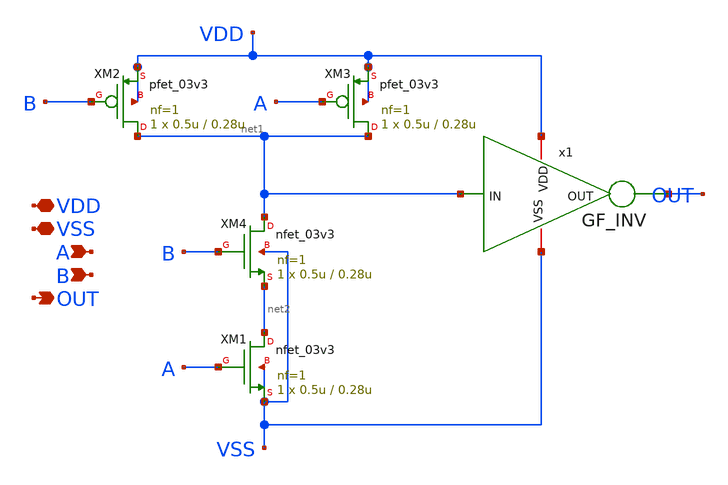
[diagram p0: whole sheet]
** sch_path: DAC_PAKISTAN_01/Pakistan1_Xschem/AND.sch
**.subckt AND VDD VSS A B OUT
*.iopin VDD
*.iopin VSS
*.ipin A
*.ipin B
*.opin OUT
XM1 net2 A VSS VSS nfet_03v3 L=0.28u W=0.5u nf=1 ad='int((nf+1)/2) * W/nf * 0.18u' as='int((nf+2)/2) * W/nf * 0.18u'
+ pd='2*int((nf+1)/2) * (W/nf + 0.18u)' ps='2*int((nf+2)/2) * (W/nf + 0.18u)' nrd='0.18u / W' nrs='0.18u / W'
+ sa=0 sb=0 sd=0 m=1
XM2 net1 B VDD VDD pfet_03v3 L=0.28u W=0.5u nf=1 ad='int((nf+1)/2) * W/nf * 0.18u' as='int((nf+2)/2) * W/nf * 0.18u'
+ pd='2*int((nf+1)/2) * (W/nf + 0.18u)' ps='2*int((nf+2)/2) * (W/nf + 0.18u)' nrd='0.18u / W' nrs='0.18u / W'
+ sa=0 sb=0 sd=0 m=1
XM3 net1 A VDD VDD pfet_03v3 L=0.28u W=0.5u nf=1 ad='int((nf+1)/2) * W/nf * 0.18u' as='int((nf+2)/2) * W/nf * 0.18u'
+ pd='2*int((nf+1)/2) * (W/nf + 0.18u)' ps='2*int((nf+2)/2) * (W/nf + 0.18u)' nrd='0.18u / W' nrs='0.18u / W'
+ sa=0 sb=0 sd=0 m=1
XM4 net1 B net2 VSS nfet_03v3 L=0.28u W=0.5u nf=1 ad='int((nf+1)/2) * W/nf * 0.18u' as='int((nf+2)/2) * W/nf * 0.18u'
+ pd='2*int((nf+1)/2) * (W/nf + 0.18u)' ps='2*int((nf+2)/2) * (W/nf + 0.18u)' nrd='0.18u / W' nrs='0.18u / W'
+ sa=0 sb=0 sd=0 m=1
x1 VSS VDD OUT net1 GF_INV
**.ends

* expanding   symbol:  GF_INV.sym # of pins=4
** sym_path: GF_INV.sym
** sch_path: GF_INV.sch
.subckt GF_INV VSS VDD OUT IN
*.iopin VDD
*.iopin VSS
*.ipin IN
*.opin OUT
XM1 OUT IN VSS VSS nfet_03v3 L=0.28u W=0.25u nf=1 ad='int((nf+1)/2) * W/nf * 0.18u' as='int((nf+2)/2) * W/nf * 0.18u'
+ pd='2*int((nf+1)/2) * (W/nf + 0.18u)' ps='2*int((nf+2)/2) * (W/nf + 0.18u)' nrd='0.18u / W' nrs='0.18u / W'
+ sa=0 sb=0 sd=0 m=1
XM2 OUT IN VDD VDD pfet_03v3 L=0.28u W=0.5u nf=1 ad='int((nf+1)/2) * W/nf * 0.18u' as='int((nf+2)/2) * W/nf * 0.18u'
+ pd='2*int((nf+1)/2) * (W/nf + 0.18u)' ps='2*int((nf+2)/2) * (W/nf + 0.18u)' nrd='0.18u / W' nrs='0.18u / W'
+ sa=0 sb=0 sd=0 m=1
.ends

.end
